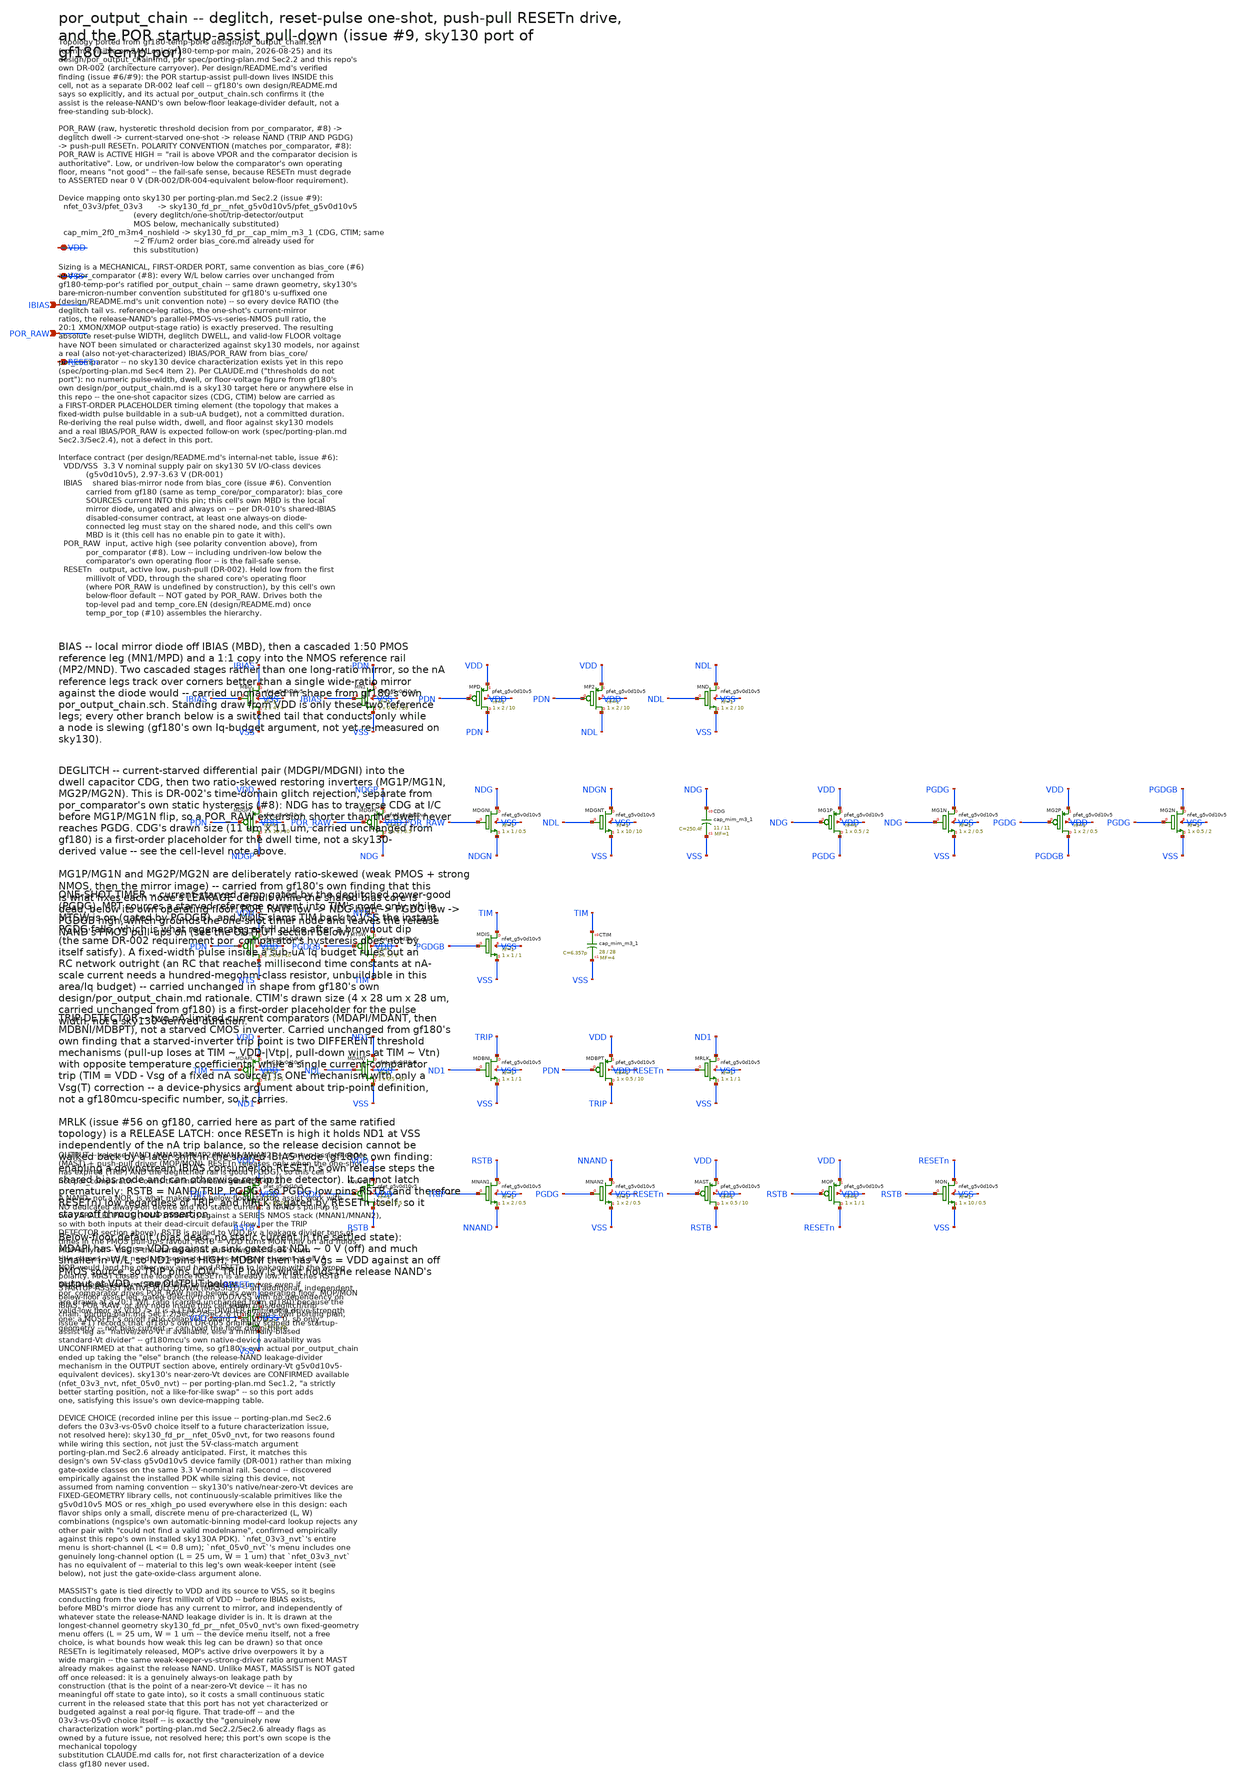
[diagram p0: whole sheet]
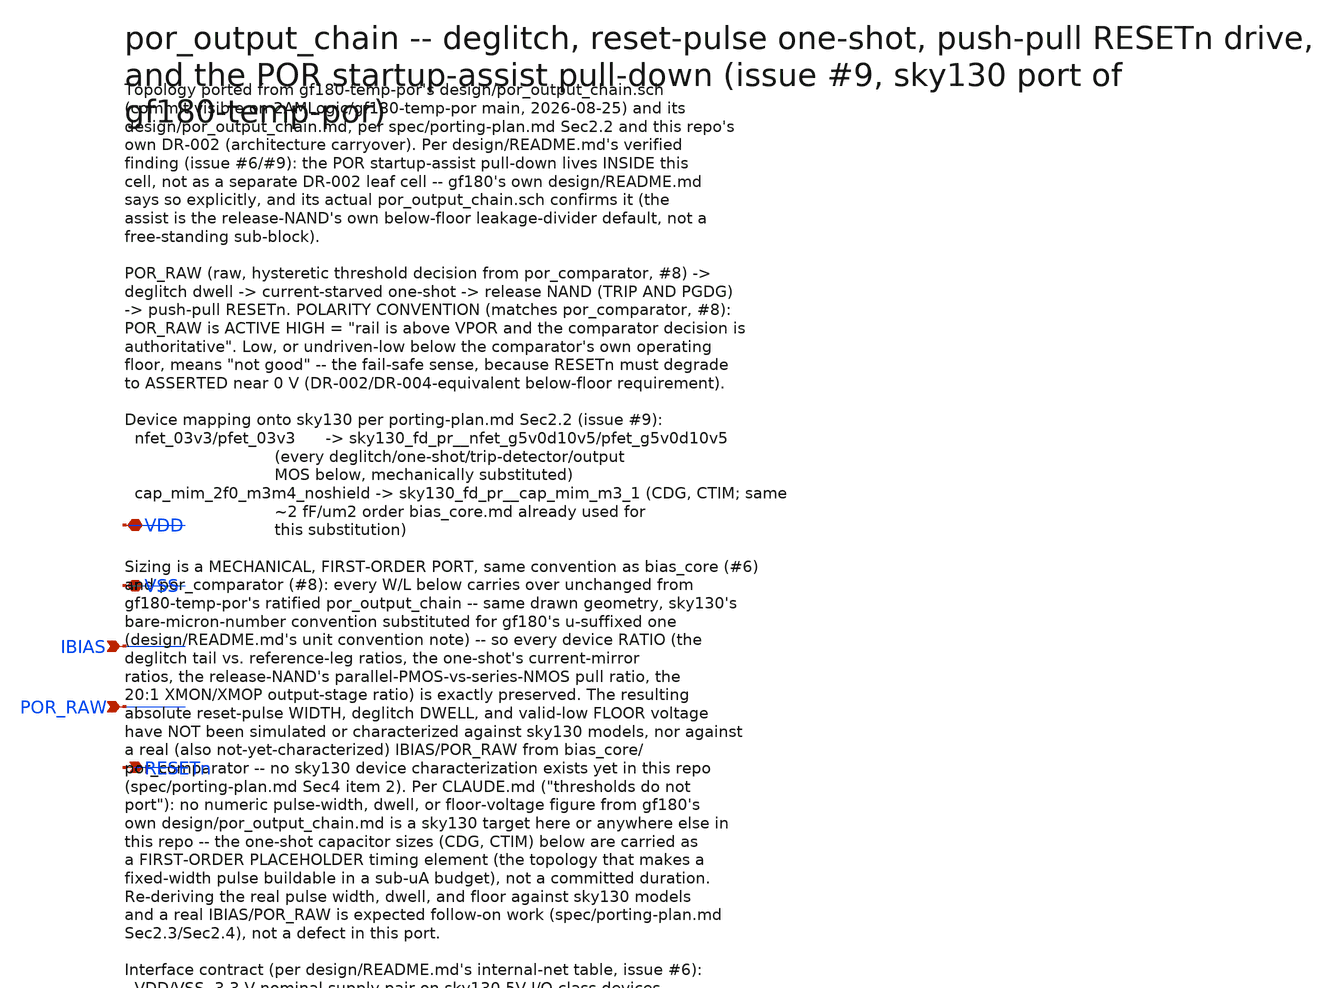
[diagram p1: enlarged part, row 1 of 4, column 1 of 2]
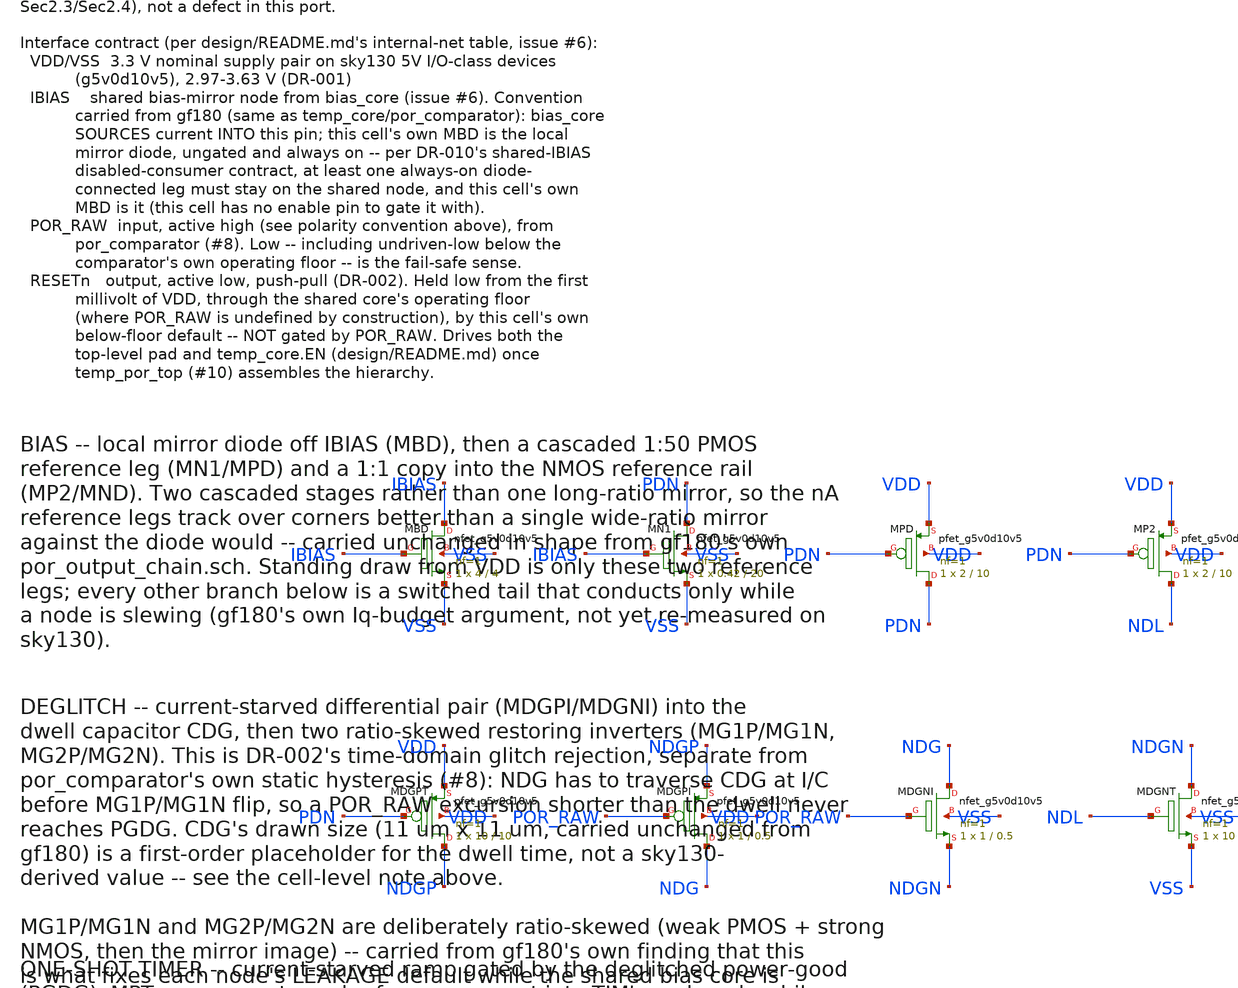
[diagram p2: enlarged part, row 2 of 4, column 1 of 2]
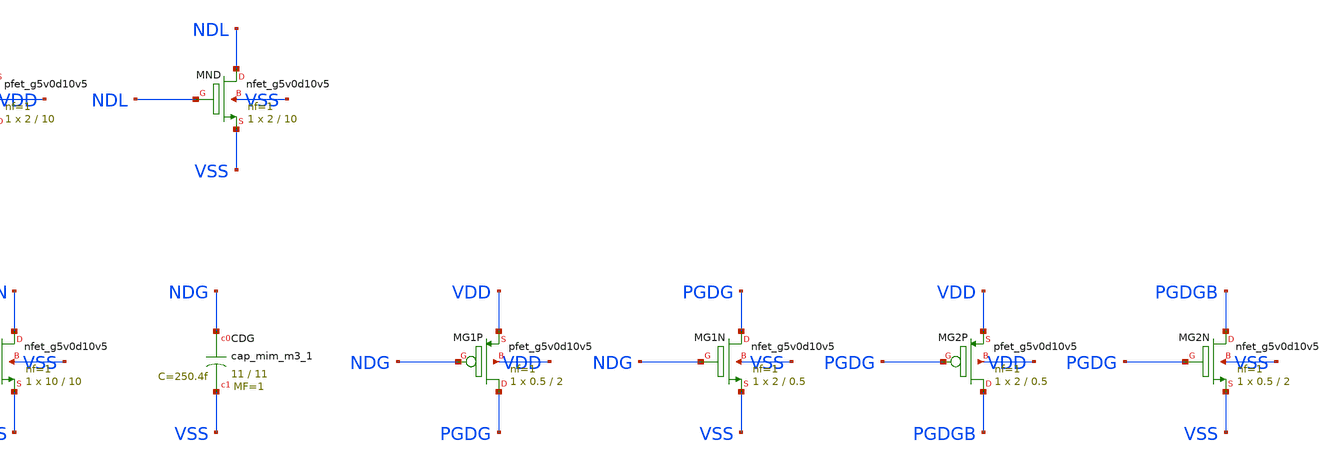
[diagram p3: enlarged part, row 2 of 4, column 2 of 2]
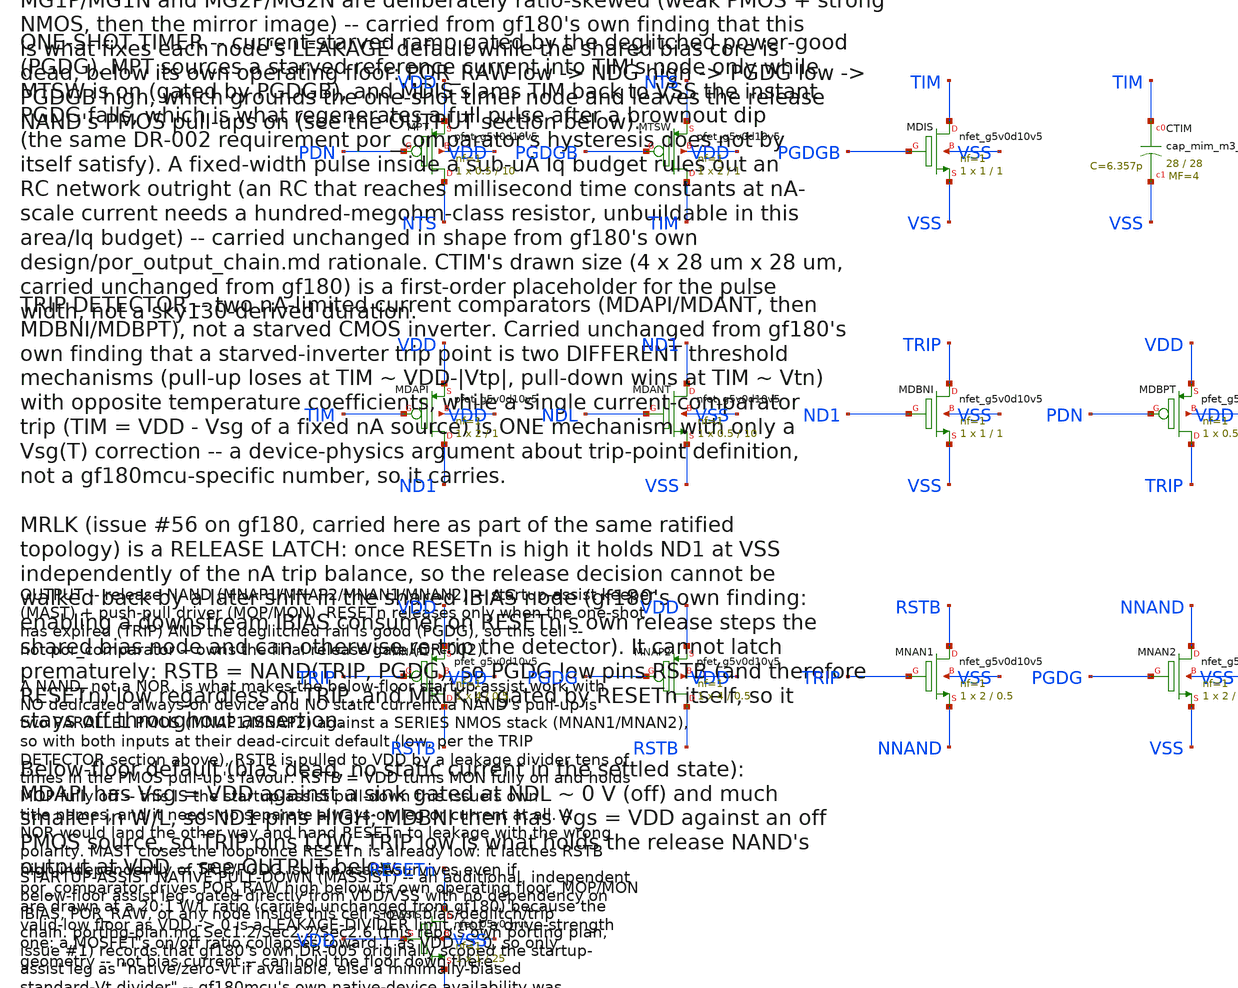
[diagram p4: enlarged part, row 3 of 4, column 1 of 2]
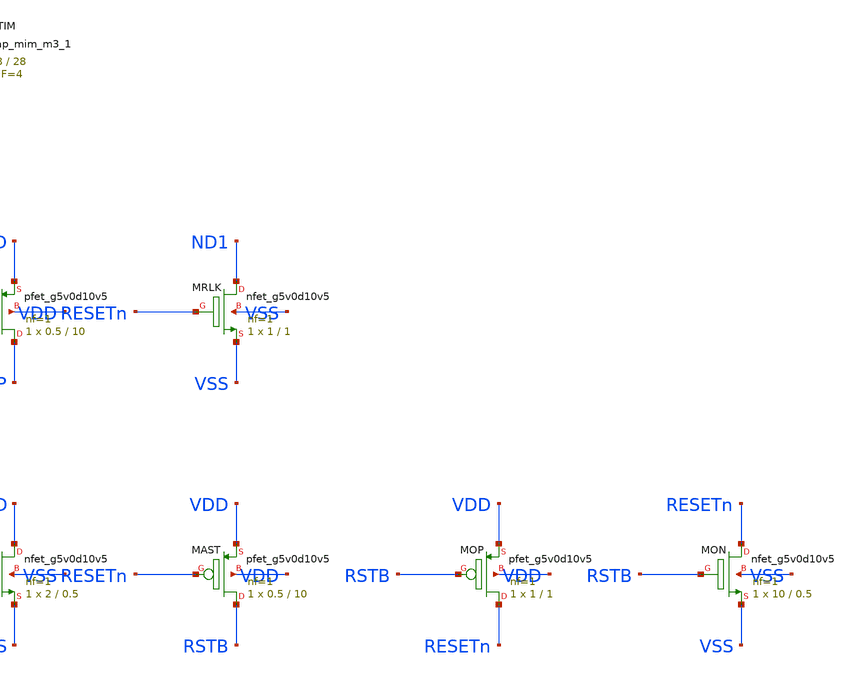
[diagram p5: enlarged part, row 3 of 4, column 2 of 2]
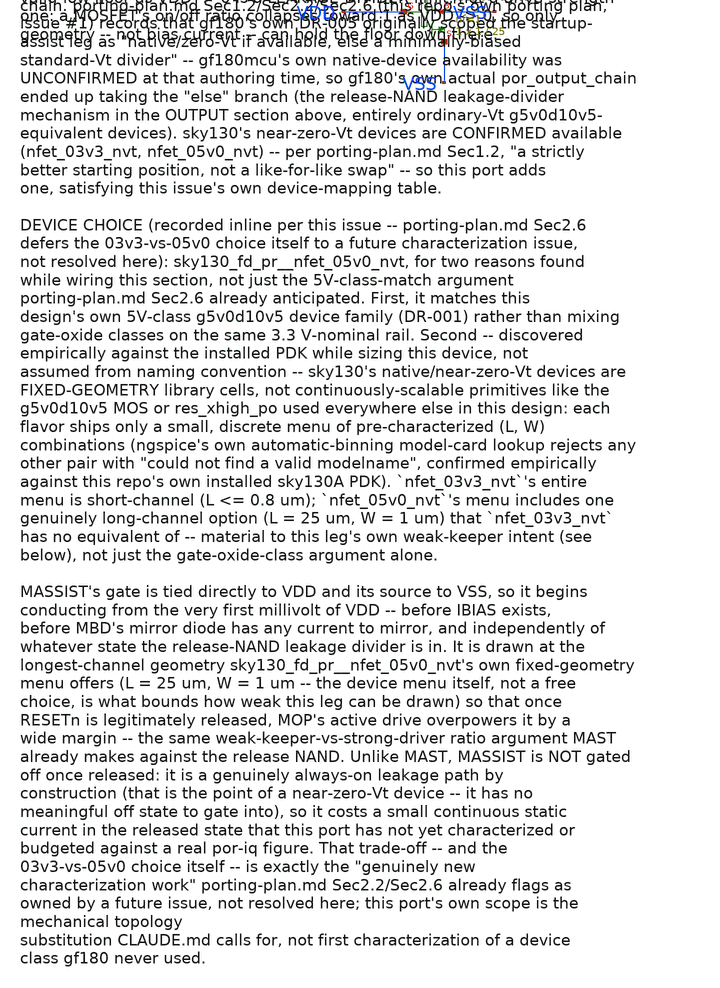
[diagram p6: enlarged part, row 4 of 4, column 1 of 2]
** sch_path: design/por_output_chain.sch
**.subckt por_output_chain VDD VSS IBIAS POR_RAW RESETn
*.iopin VDD
*.iopin VSS
*.ipin IBIAS
*.ipin POR_RAW
*.opin RESETn
XMBD IBIAS IBIAS VSS VSS sky130_fd_pr__nfet_g5v0d10v5 L=4 W=4 nf=1 ad='int((1 + 1)/2) * 4 / 1 * 0.29'
+ as='int((1 + 2)/2) * 4 / 1 * 0.29' pd='2*int((1 + 1)/2) * (4 / 1 + 0.29)' ps='2*int((1 + 2)/2) * (4 / 1 + 0.29)'
+ nrd='0.29 / 4 ' nrs='0.29 / 4 ' sa=0 sb=0 sd=0 mult=1 m=1
XMN1 PDN IBIAS VSS VSS sky130_fd_pr__nfet_g5v0d10v5 L=20 W=0.42 nf=1 ad='int((1 + 1)/2) * 0.42 / 1 * 0.29'
+ as='int((1 + 2)/2) * 0.42 / 1 * 0.29' pd='2*int((1 + 1)/2) * (0.42 / 1 + 0.29)' ps='2*int((1 + 2)/2) * (0.42 / 1 + 0.29)'
+ nrd='0.29 / 0.42 ' nrs='0.29 / 0.42 ' sa=0 sb=0 sd=0 mult=1 m=1
XMPD PDN PDN VDD VDD sky130_fd_pr__pfet_g5v0d10v5 L=10 W=2 nf=1 ad='int((1 + 1)/2) * 2 / 1 * 0.29' as='int((1 + 2)/2) * 2 / 1 * 0.29'
+ pd='2*int((1 + 1)/2) * (2 / 1 + 0.29)' ps='2*int((1 + 2)/2) * (2 / 1 + 0.29)' nrd='0.29 / 2 ' nrs='0.29 / 2 '
+ sa=0 sb=0 sd=0 mult=1 m=1
XMP2 NDL PDN VDD VDD sky130_fd_pr__pfet_g5v0d10v5 L=10 W=2 nf=1 ad='int((1 + 1)/2) * 2 / 1 * 0.29' as='int((1 + 2)/2) * 2 / 1 * 0.29'
+ pd='2*int((1 + 1)/2) * (2 / 1 + 0.29)' ps='2*int((1 + 2)/2) * (2 / 1 + 0.29)' nrd='0.29 / 2 ' nrs='0.29 / 2 '
+ sa=0 sb=0 sd=0 mult=1 m=1
XMND NDL NDL VSS VSS sky130_fd_pr__nfet_g5v0d10v5 L=10 W=2 nf=1 ad='int((1 + 1)/2) * 2 / 1 * 0.29' as='int((1 + 2)/2) * 2 / 1 * 0.29'
+ pd='2*int((1 + 1)/2) * (2 / 1 + 0.29)' ps='2*int((1 + 2)/2) * (2 / 1 + 0.29)' nrd='0.29 / 2 ' nrs='0.29 / 2 '
+ sa=0 sb=0 sd=0 mult=1 m=1
XMDGPT NDGP PDN VDD VDD sky130_fd_pr__pfet_g5v0d10v5 L=10 W=10 nf=1 ad='int((1 + 1)/2) * 10 / 1 * 0.29'
+ as='int((1 + 2)/2) * 10 / 1 * 0.29' pd='2*int((1 + 1)/2) * (10 / 1 + 0.29)' ps='2*int((1 + 2)/2) * (10 / 1 + 0.29)'
+ nrd='0.29 / 10 ' nrs='0.29 / 10 ' sa=0 sb=0 sd=0 mult=1 m=1
XMDGPI NDG POR_RAW NDGP VDD sky130_fd_pr__pfet_g5v0d10v5 L=0.5 W=1 nf=1 ad='int((1 + 1)/2) * 1 / 1 * 0.29'
+ as='int((1 + 2)/2) * 1 / 1 * 0.29' pd='2*int((1 + 1)/2) * (1 / 1 + 0.29)' ps='2*int((1 + 2)/2) * (1 / 1 + 0.29)'
+ nrd='0.29 / 1 ' nrs='0.29 / 1 ' sa=0 sb=0 sd=0 mult=1 m=1
XMDGNI NDG POR_RAW NDGN VSS sky130_fd_pr__nfet_g5v0d10v5 L=0.5 W=1 nf=1 ad='int((1 + 1)/2) * 1 / 1 * 0.29'
+ as='int((1 + 2)/2) * 1 / 1 * 0.29' pd='2*int((1 + 1)/2) * (1 / 1 + 0.29)' ps='2*int((1 + 2)/2) * (1 / 1 + 0.29)'
+ nrd='0.29 / 1 ' nrs='0.29 / 1 ' sa=0 sb=0 sd=0 mult=1 m=1
XMDGNT NDGN NDL VSS VSS sky130_fd_pr__nfet_g5v0d10v5 L=10 W=10 nf=1 ad='int((1 + 1)/2) * 10 / 1 * 0.29'
+ as='int((1 + 2)/2) * 10 / 1 * 0.29' pd='2*int((1 + 1)/2) * (10 / 1 + 0.29)' ps='2*int((1 + 2)/2) * (10 / 1 + 0.29)'
+ nrd='0.29 / 10 ' nrs='0.29 / 10 ' sa=0 sb=0 sd=0 mult=1 m=1
XCDG NDG VSS sky130_fd_pr__cap_mim_m3_1 W=11 L=11 MF=1 m=1
XMG1P PGDG NDG VDD VDD sky130_fd_pr__pfet_g5v0d10v5 L=2 W=0.5 nf=1 ad='int((1 + 1)/2) * 0.5 / 1 * 0.29'
+ as='int((1 + 2)/2) * 0.5 / 1 * 0.29' pd='2*int((1 + 1)/2) * (0.5 / 1 + 0.29)' ps='2*int((1 + 2)/2) * (0.5 / 1 + 0.29)'
+ nrd='0.29 / 0.5 ' nrs='0.29 / 0.5 ' sa=0 sb=0 sd=0 mult=1 m=1
XMG1N PGDG NDG VSS VSS sky130_fd_pr__nfet_g5v0d10v5 L=0.5 W=2 nf=1 ad='int((1 + 1)/2) * 2 / 1 * 0.29'
+ as='int((1 + 2)/2) * 2 / 1 * 0.29' pd='2*int((1 + 1)/2) * (2 / 1 + 0.29)' ps='2*int((1 + 2)/2) * (2 / 1 + 0.29)'
+ nrd='0.29 / 2 ' nrs='0.29 / 2 ' sa=0 sb=0 sd=0 mult=1 m=1
XMG2P PGDGB PGDG VDD VDD sky130_fd_pr__pfet_g5v0d10v5 L=0.5 W=2 nf=1 ad='int((1 + 1)/2) * 2 / 1 * 0.29'
+ as='int((1 + 2)/2) * 2 / 1 * 0.29' pd='2*int((1 + 1)/2) * (2 / 1 + 0.29)' ps='2*int((1 + 2)/2) * (2 / 1 + 0.29)'
+ nrd='0.29 / 2 ' nrs='0.29 / 2 ' sa=0 sb=0 sd=0 mult=1 m=1
XMG2N PGDGB PGDG VSS VSS sky130_fd_pr__nfet_g5v0d10v5 L=2 W=0.5 nf=1 ad='int((1 + 1)/2) * 0.5 / 1 * 0.29'
+ as='int((1 + 2)/2) * 0.5 / 1 * 0.29' pd='2*int((1 + 1)/2) * (0.5 / 1 + 0.29)' ps='2*int((1 + 2)/2) * (0.5 / 1 + 0.29)'
+ nrd='0.29 / 0.5 ' nrs='0.29 / 0.5 ' sa=0 sb=0 sd=0 mult=1 m=1
XMPT NTS PDN VDD VDD sky130_fd_pr__pfet_g5v0d10v5 L=10 W=0.5 nf=1 ad='int((1 + 1)/2) * 0.5 / 1 * 0.29'
+ as='int((1 + 2)/2) * 0.5 / 1 * 0.29' pd='2*int((1 + 1)/2) * (0.5 / 1 + 0.29)' ps='2*int((1 + 2)/2) * (0.5 / 1 + 0.29)'
+ nrd='0.29 / 0.5 ' nrs='0.29 / 0.5 ' sa=0 sb=0 sd=0 mult=1 m=1
XMTSW TIM PGDGB NTS VDD sky130_fd_pr__pfet_g5v0d10v5 L=1 W=2 nf=1 ad='int((1 + 1)/2) * 2 / 1 * 0.29'
+ as='int((1 + 2)/2) * 2 / 1 * 0.29' pd='2*int((1 + 1)/2) * (2 / 1 + 0.29)' ps='2*int((1 + 2)/2) * (2 / 1 + 0.29)'
+ nrd='0.29 / 2 ' nrs='0.29 / 2 ' sa=0 sb=0 sd=0 mult=1 m=1
XMDIS TIM PGDGB VSS VSS sky130_fd_pr__nfet_g5v0d10v5 L=1 W=1 nf=1 ad='int((1 + 1)/2) * 1 / 1 * 0.29'
+ as='int((1 + 2)/2) * 1 / 1 * 0.29' pd='2*int((1 + 1)/2) * (1 / 1 + 0.29)' ps='2*int((1 + 2)/2) * (1 / 1 + 0.29)'
+ nrd='0.29 / 1 ' nrs='0.29 / 1 ' sa=0 sb=0 sd=0 mult=1 m=1
XCTIM TIM VSS sky130_fd_pr__cap_mim_m3_1 W=28 L=28 MF=4 m=4
XMDAPI ND1 TIM VDD VDD sky130_fd_pr__pfet_g5v0d10v5 L=1 W=2 nf=1 ad='int((1 + 1)/2) * 2 / 1 * 0.29' as='int((1 + 2)/2) * 2 / 1 * 0.29'
+ pd='2*int((1 + 1)/2) * (2 / 1 + 0.29)' ps='2*int((1 + 2)/2) * (2 / 1 + 0.29)' nrd='0.29 / 2 ' nrs='0.29 / 2 '
+ sa=0 sb=0 sd=0 mult=1 m=1
XMDANT ND1 NDL VSS VSS sky130_fd_pr__nfet_g5v0d10v5 L=10 W=0.5 nf=1 ad='int((1 + 1)/2) * 0.5 / 1 * 0.29'
+ as='int((1 + 2)/2) * 0.5 / 1 * 0.29' pd='2*int((1 + 1)/2) * (0.5 / 1 + 0.29)' ps='2*int((1 + 2)/2) * (0.5 / 1 + 0.29)'
+ nrd='0.29 / 0.5 ' nrs='0.29 / 0.5 ' sa=0 sb=0 sd=0 mult=1 m=1
XMDBNI TRIP ND1 VSS VSS sky130_fd_pr__nfet_g5v0d10v5 L=1 W=1 nf=1 ad='int((1 + 1)/2) * 1 / 1 * 0.29'
+ as='int((1 + 2)/2) * 1 / 1 * 0.29' pd='2*int((1 + 1)/2) * (1 / 1 + 0.29)' ps='2*int((1 + 2)/2) * (1 / 1 + 0.29)'
+ nrd='0.29 / 1 ' nrs='0.29 / 1 ' sa=0 sb=0 sd=0 mult=1 m=1
XMDBPT TRIP PDN VDD VDD sky130_fd_pr__pfet_g5v0d10v5 L=10 W=0.5 nf=1 ad='int((1 + 1)/2) * 0.5 / 1 * 0.29'
+ as='int((1 + 2)/2) * 0.5 / 1 * 0.29' pd='2*int((1 + 1)/2) * (0.5 / 1 + 0.29)' ps='2*int((1 + 2)/2) * (0.5 / 1 + 0.29)'
+ nrd='0.29 / 0.5 ' nrs='0.29 / 0.5 ' sa=0 sb=0 sd=0 mult=1 m=1
XMRLK ND1 RESETn VSS VSS sky130_fd_pr__nfet_g5v0d10v5 L=1 W=1 nf=1 ad='int((1 + 1)/2) * 1 / 1 * 0.29'
+ as='int((1 + 2)/2) * 1 / 1 * 0.29' pd='2*int((1 + 1)/2) * (1 / 1 + 0.29)' ps='2*int((1 + 2)/2) * (1 / 1 + 0.29)'
+ nrd='0.29 / 1 ' nrs='0.29 / 1 ' sa=0 sb=0 sd=0 mult=1 m=1
XMNAP1 RSTB TRIP VDD VDD sky130_fd_pr__pfet_g5v0d10v5 L=0.5 W=4 nf=1 ad='int((1 + 1)/2) * 4 / 1 * 0.29'
+ as='int((1 + 2)/2) * 4 / 1 * 0.29' pd='2*int((1 + 1)/2) * (4 / 1 + 0.29)' ps='2*int((1 + 2)/2) * (4 / 1 + 0.29)'
+ nrd='0.29 / 4 ' nrs='0.29 / 4 ' sa=0 sb=0 sd=0 mult=1 m=1
XMNAP2 RSTB PGDG VDD VDD sky130_fd_pr__pfet_g5v0d10v5 L=0.5 W=4 nf=1 ad='int((1 + 1)/2) * 4 / 1 * 0.29'
+ as='int((1 + 2)/2) * 4 / 1 * 0.29' pd='2*int((1 + 1)/2) * (4 / 1 + 0.29)' ps='2*int((1 + 2)/2) * (4 / 1 + 0.29)'
+ nrd='0.29 / 4 ' nrs='0.29 / 4 ' sa=0 sb=0 sd=0 mult=1 m=1
XMNAN1 RSTB TRIP NNAND VSS sky130_fd_pr__nfet_g5v0d10v5 L=0.5 W=2 nf=1 ad='int((1 + 1)/2) * 2 / 1 * 0.29'
+ as='int((1 + 2)/2) * 2 / 1 * 0.29' pd='2*int((1 + 1)/2) * (2 / 1 + 0.29)' ps='2*int((1 + 2)/2) * (2 / 1 + 0.29)'
+ nrd='0.29 / 2 ' nrs='0.29 / 2 ' sa=0 sb=0 sd=0 mult=1 m=1
XMNAN2 NNAND PGDG VSS VSS sky130_fd_pr__nfet_g5v0d10v5 L=0.5 W=2 nf=1 ad='int((1 + 1)/2) * 2 / 1 * 0.29'
+ as='int((1 + 2)/2) * 2 / 1 * 0.29' pd='2*int((1 + 1)/2) * (2 / 1 + 0.29)' ps='2*int((1 + 2)/2) * (2 / 1 + 0.29)'
+ nrd='0.29 / 2 ' nrs='0.29 / 2 ' sa=0 sb=0 sd=0 mult=1 m=1
XMAST RSTB RESETn VDD VDD sky130_fd_pr__pfet_g5v0d10v5 L=10 W=0.5 nf=1 ad='int((1 + 1)/2) * 0.5 / 1 * 0.29'
+ as='int((1 + 2)/2) * 0.5 / 1 * 0.29' pd='2*int((1 + 1)/2) * (0.5 / 1 + 0.29)' ps='2*int((1 + 2)/2) * (0.5 / 1 + 0.29)'
+ nrd='0.29 / 0.5 ' nrs='0.29 / 0.5 ' sa=0 sb=0 sd=0 mult=1 m=1
XMOP RESETn RSTB VDD VDD sky130_fd_pr__pfet_g5v0d10v5 L=1 W=1 nf=1 ad='int((1 + 1)/2) * 1 / 1 * 0.29'
+ as='int((1 + 2)/2) * 1 / 1 * 0.29' pd='2*int((1 + 1)/2) * (1 / 1 + 0.29)' ps='2*int((1 + 2)/2) * (1 / 1 + 0.29)'
+ nrd='0.29 / 1 ' nrs='0.29 / 1 ' sa=0 sb=0 sd=0 mult=1 m=1
XMON RESETn RSTB VSS VSS sky130_fd_pr__nfet_g5v0d10v5 L=0.5 W=10 nf=1 ad='int((1 + 1)/2) * 10 / 1 * 0.29'
+ as='int((1 + 2)/2) * 10 / 1 * 0.29' pd='2*int((1 + 1)/2) * (10 / 1 + 0.29)' ps='2*int((1 + 2)/2) * (10 / 1 + 0.29)'
+ nrd='0.29 / 10 ' nrs='0.29 / 10 ' sa=0 sb=0 sd=0 mult=1 m=1
XMASSIST RESETn VDD VSS VSS sky130_fd_pr__nfet_05v0_nvt L=25 W=1 nf=1 ad='int((1 + 1)/2) * 1 / 1 * 0.29'
+ as='int((1 + 2)/2) * 1 / 1 * 0.29' pd='2*int((1 + 1)/2) * (1 / 1 + 0.29)' ps='2*int((1 + 2)/2) * (1 / 1 + 0.29)'
+ nrd='0.29 / 1 ' nrs='0.29 / 1 ' sa=0 sb=0 sd=0 mult=1 m=1
**.ends
.end
